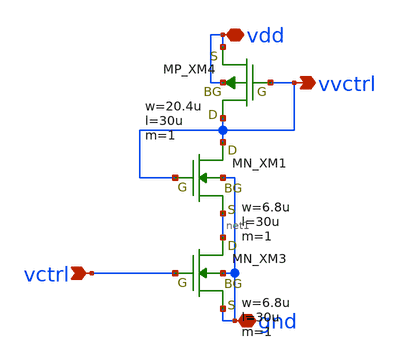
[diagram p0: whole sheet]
** sch_path: member_project/ringOSC/noritsuna/CS.sch
**.subckt CS vdd vvctrl gnd vctrl
*.iopin vdd
*.opin vvctrl
*.iopin gnd
*.ipin vctrl
XM3 net1 vctrl gnd gnd NMOS w=6.8u l=30u as=0 ad=0 ps=0 pd=0 nrd=0 nrs=0 m=1
XM4 vvctrl vvctrl vdd vdd PMOS w=20.4u l=30u as=0 ad=0 ps=0 pd=0 nrd=0 nrs=0 m=1
XM1 vvctrl vvctrl net1 gnd NMOS w=6.8u l=30u as=0 ad=0 ps=0 pd=0 nrd=0 nrs=0 m=1
**.ends
.end
